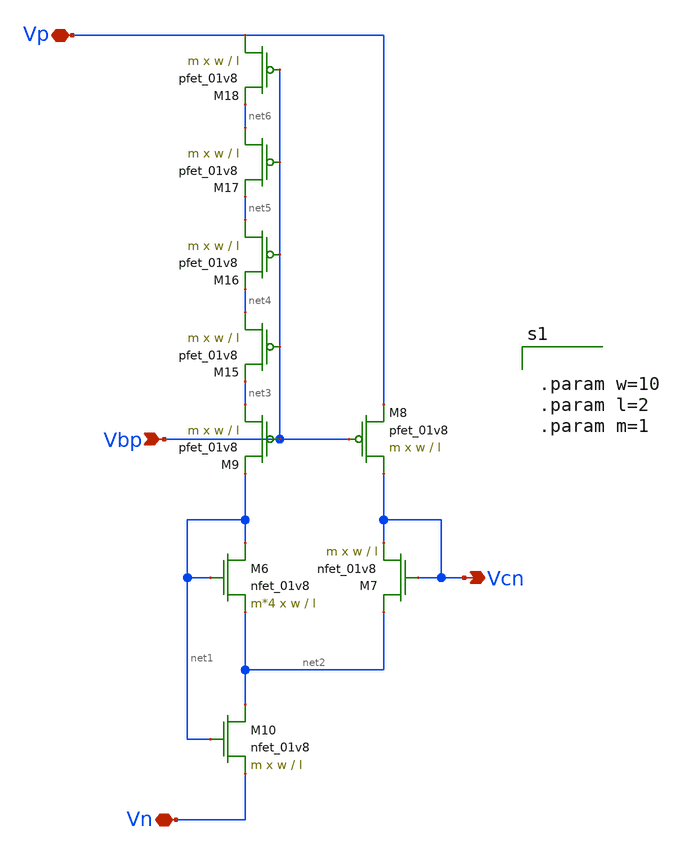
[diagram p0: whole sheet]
** sch_path: schematic/old/cascode_generator.sch
**.subckt cascode_generator Vbp Vn Vp Vcn
*.ipin Vbp
*.iopin Vn
*.iopin Vp
*.opin Vcn
XM6 net1 net1 net2 GND sky130_fd_pr__nfet_01v8 L=l W=w nf=1 ad='int((nf+1)/2) * W/nf * 0.29' as='int((nf+2)/2) * W/nf * 0.29'
+ pd='2*int((nf+1)/2) * (W/nf + 0.29)' ps='2*int((nf+2)/2) * (W/nf + 0.29)' nrd='0.29 / W' nrs='0.29 / W'
+ sa=0 sb=0 sd=0 mult=m*4 m=m*4
XM7 net2 Vcn Vcn GND sky130_fd_pr__nfet_01v8 L=l W=w nf=1 ad='int((nf+1)/2) * W/nf * 0.29' as='int((nf+2)/2) * W/nf * 0.29'
+ pd='2*int((nf+1)/2) * (W/nf + 0.29)' ps='2*int((nf+2)/2) * (W/nf + 0.29)' nrd='0.29 / W' nrs='0.29 / W'
+ sa=0 sb=0 sd=0 mult=m m=m
XM8 Vcn Vbp Vp VDD sky130_fd_pr__pfet_01v8 L=l W=w nf=1 ad='int((nf+1)/2) * W/nf * 0.29' as='int((nf+2)/2) * W/nf * 0.29'
+ pd='2*int((nf+1)/2) * (W/nf + 0.29)' ps='2*int((nf+2)/2) * (W/nf + 0.29)' nrd='0.29 / W' nrs='0.29 / W'
+ sa=0 sb=0 sd=0 mult=m m=m
XM9 net3 Vbp net1 VDD sky130_fd_pr__pfet_01v8 L=l W=w nf=1 ad='int((nf+1)/2) * W/nf * 0.29' as='int((nf+2)/2) * W/nf * 0.29'
+ pd='2*int((nf+1)/2) * (W/nf + 0.29)' ps='2*int((nf+2)/2) * (W/nf + 0.29)' nrd='0.29 / W' nrs='0.29 / W'
+ sa=0 sb=0 sd=0 mult=m m=m
XM10 net2 net1 Vn GND sky130_fd_pr__nfet_01v8 L=l W=w nf=1 ad='int((nf+1)/2) * W/nf * 0.29' as='int((nf+2)/2) * W/nf * 0.29'
+ pd='2*int((nf+1)/2) * (W/nf + 0.29)' ps='2*int((nf+2)/2) * (W/nf + 0.29)' nrd='0.29 / W' nrs='0.29 / W'
+ sa=0 sb=0 sd=0 mult=m m=m
XM15 net4 Vbp net3 VDD sky130_fd_pr__pfet_01v8 L=l W=w nf=1 ad='int((nf+1)/2) * W/nf * 0.29' as='int((nf+2)/2) * W/nf * 0.29'
+ pd='2*int((nf+1)/2) * (W/nf + 0.29)' ps='2*int((nf+2)/2) * (W/nf + 0.29)' nrd='0.29 / W' nrs='0.29 / W'
+ sa=0 sb=0 sd=0 mult=m m=m
XM16 net5 Vbp net4 VDD sky130_fd_pr__pfet_01v8 L=l W=w nf=1 ad='int((nf+1)/2) * W/nf * 0.29' as='int((nf+2)/2) * W/nf * 0.29'
+ pd='2*int((nf+1)/2) * (W/nf + 0.29)' ps='2*int((nf+2)/2) * (W/nf + 0.29)' nrd='0.29 / W' nrs='0.29 / W'
+ sa=0 sb=0 sd=0 mult=m m=m
XM17 net6 Vbp net5 VDD sky130_fd_pr__pfet_01v8 L=l W=w nf=1 ad='int((nf+1)/2) * W/nf * 0.29' as='int((nf+2)/2) * W/nf * 0.29'
+ pd='2*int((nf+1)/2) * (W/nf + 0.29)' ps='2*int((nf+2)/2) * (W/nf + 0.29)' nrd='0.29 / W' nrs='0.29 / W'
+ sa=0 sb=0 sd=0 mult=m m=m
XM18 Vp Vbp net6 VDD sky130_fd_pr__pfet_01v8 L=l W=w nf=1 ad='int((nf+1)/2) * W/nf * 0.29' as='int((nf+2)/2) * W/nf * 0.29'
+ pd='2*int((nf+1)/2) * (W/nf + 0.29)' ps='2*int((nf+2)/2) * (W/nf + 0.29)' nrd='0.29 / W' nrs='0.29 / W'
+ sa=0 sb=0 sd=0 mult=m m=m
**** begin user architecture code


.param w=10
.param l=2
.param m=1


**** end user architecture code
**.ends
.end
